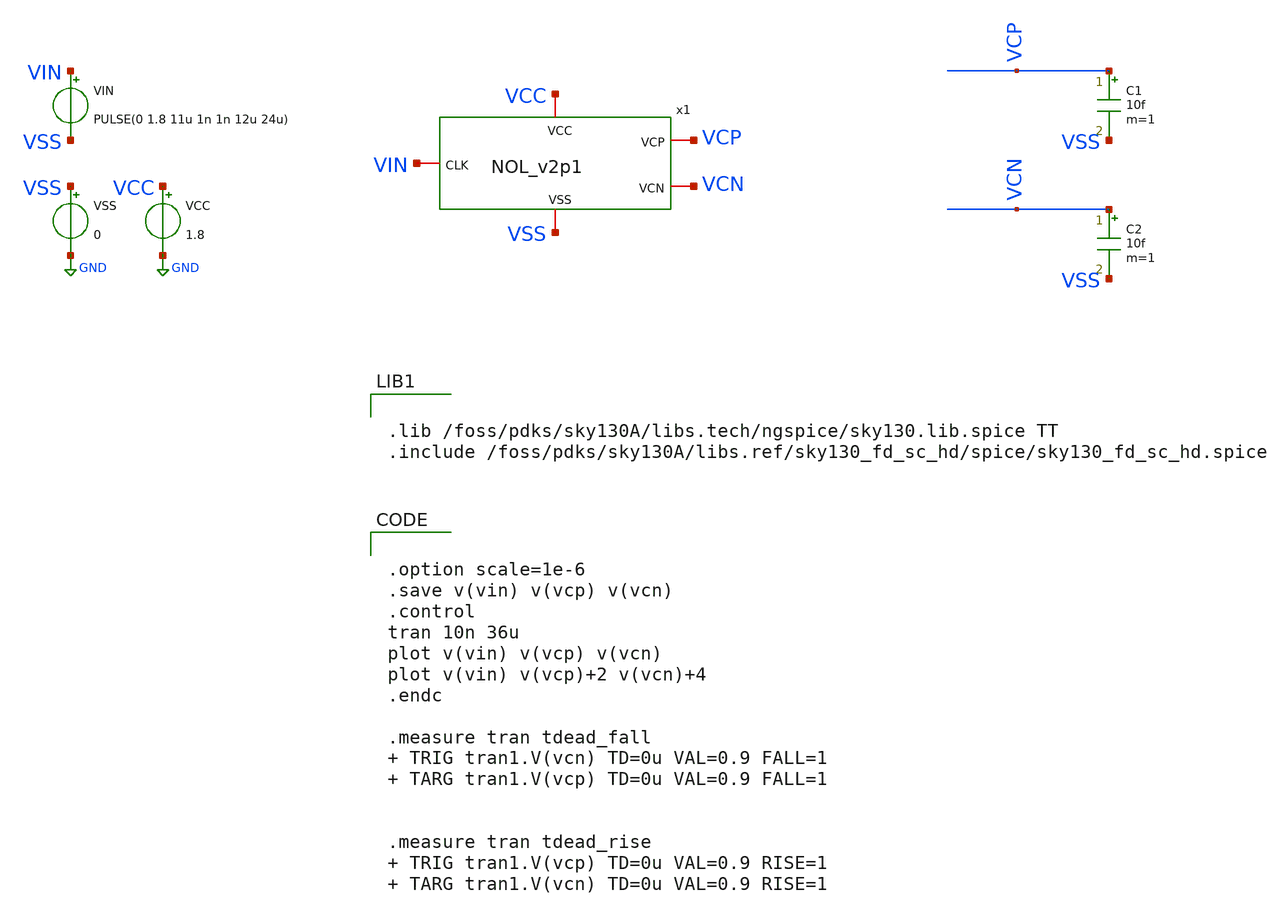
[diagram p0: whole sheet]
** sch_path: xschem/tb_NOL_v2p1.sch
**.subckt tb_NOL_v2p1
VCC VCC GND 1.8
VSS VSS GND 0
VIN VIN VSS PULSE(0 1.8 11u 1n 1n 12u 24u)
C1 VCP VSS 10f m=1
C2 VCN VSS 10f m=1
x1 VCC VSS VCP VIN VCN NOL_v2p1
**** begin user architecture code


.lib /foss/pdks/sky130A/libs.tech/ngspice/sky130.lib.spice TT
.include /foss/pdks/sky130A/libs.ref/sky130_fd_sc_hd/spice/sky130_fd_sc_hd.spice




.option scale=1e-6
.save v(vin) v(vcp) v(vcn)
.control
tran 10n 36u
plot v(vin) v(vcp) v(vcn)
plot v(vin) v(vcp)+2 v(vcn)+4
.endc

.measure tran tdead_fall  TRIG tran1.V(vcn) TD=0u VAL=0.9 FALL=1  TARG tran1.V(vcp) TD=0u VAL=0.9
+ FALL=1


.measure tran tdead_rise  TRIG tran1.V(vcp) TD=0u VAL=0.9 RISE=1  TARG tran1.V(vcn) TD=0u VAL=0.9
+ RISE=1




**** end user architecture code
**.ends
.GLOBAL GND
.end
